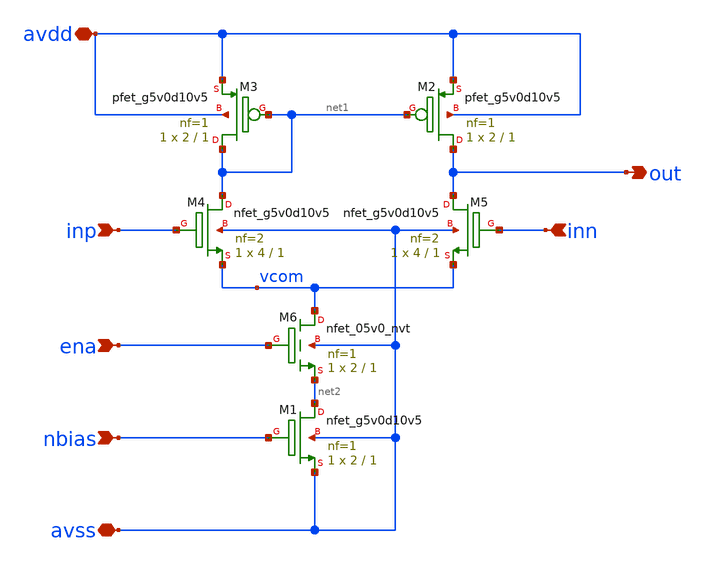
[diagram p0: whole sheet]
** sch_path: xschem/bias_amp.sch
**.subckt bias_amp inp nbias inn out avdd avss ena
*.ipin inp
*.ipin nbias
*.ipin inn
*.opin out
*.iopin avdd
*.iopin avss
*.ipin ena
XM1 net2 nbias avss avss sky130_fd_pr__nfet_g5v0d10v5 L=1 W=2 nf=1 ad='int((nf+1)/2) * W/nf * 0.29' as='int((nf+2)/2) * W/nf * 0.29'
+ pd='2*int((nf+1)/2) * (W/nf + 0.29)' ps='2*int((nf+2)/2) * (W/nf + 0.29)' nrd='0.29 / W' nrs='0.29 / W'
+ sa=0 sb=0 sd=0 mult=1 m=1
XM2 out net1 avdd avdd sky130_fd_pr__pfet_g5v0d10v5 L=1 W=2 nf=1 ad='int((nf+1)/2) * W/nf * 0.29' as='int((nf+2)/2) * W/nf * 0.29'
+ pd='2*int((nf+1)/2) * (W/nf + 0.29)' ps='2*int((nf+2)/2) * (W/nf + 0.29)' nrd='0.29 / W' nrs='0.29 / W'
+ sa=0 sb=0 sd=0 mult=1 m=1
XM3 net1 net1 avdd avdd sky130_fd_pr__pfet_g5v0d10v5 L=1 W=2 nf=1 ad='int((nf+1)/2) * W/nf * 0.29' as='int((nf+2)/2) * W/nf * 0.29'
+ pd='2*int((nf+1)/2) * (W/nf + 0.29)' ps='2*int((nf+2)/2) * (W/nf + 0.29)' nrd='0.29 / W' nrs='0.29 / W'
+ sa=0 sb=0 sd=0 mult=1 m=1
XM4 net1 inp vcom avss sky130_fd_pr__nfet_g5v0d10v5 L=1 W=4 nf=2 ad='int((nf+1)/2) * W/nf * 0.29' as='int((nf+2)/2) * W/nf * 0.29'
+ pd='2*int((nf+1)/2) * (W/nf + 0.29)' ps='2*int((nf+2)/2) * (W/nf + 0.29)' nrd='0.29 / W' nrs='0.29 / W'
+ sa=0 sb=0 sd=0 mult=1 m=1
XM5 out inn vcom avss sky130_fd_pr__nfet_g5v0d10v5 L=1 W=4 nf=2 ad='int((nf+1)/2) * W/nf * 0.29' as='int((nf+2)/2) * W/nf * 0.29'
+ pd='2*int((nf+1)/2) * (W/nf + 0.29)' ps='2*int((nf+2)/2) * (W/nf + 0.29)' nrd='0.29 / W' nrs='0.29 / W'
+ sa=0 sb=0 sd=0 mult=1 m=1
XM6 vcom ena net2 avss sky130_fd_pr__nfet_05v0_nvt L=1 W=2 nf=1 ad='int((nf+1)/2) * W/nf * 0.29' as='int((nf+2)/2) * W/nf * 0.29'
+ pd='2*int((nf+1)/2) * (W/nf + 0.29)' ps='2*int((nf+2)/2) * (W/nf + 0.29)' nrd='0.29 / W' nrs='0.29 / W'
+ sa=0 sb=0 sd=0 mult=1 m=1
**.ends
.end
